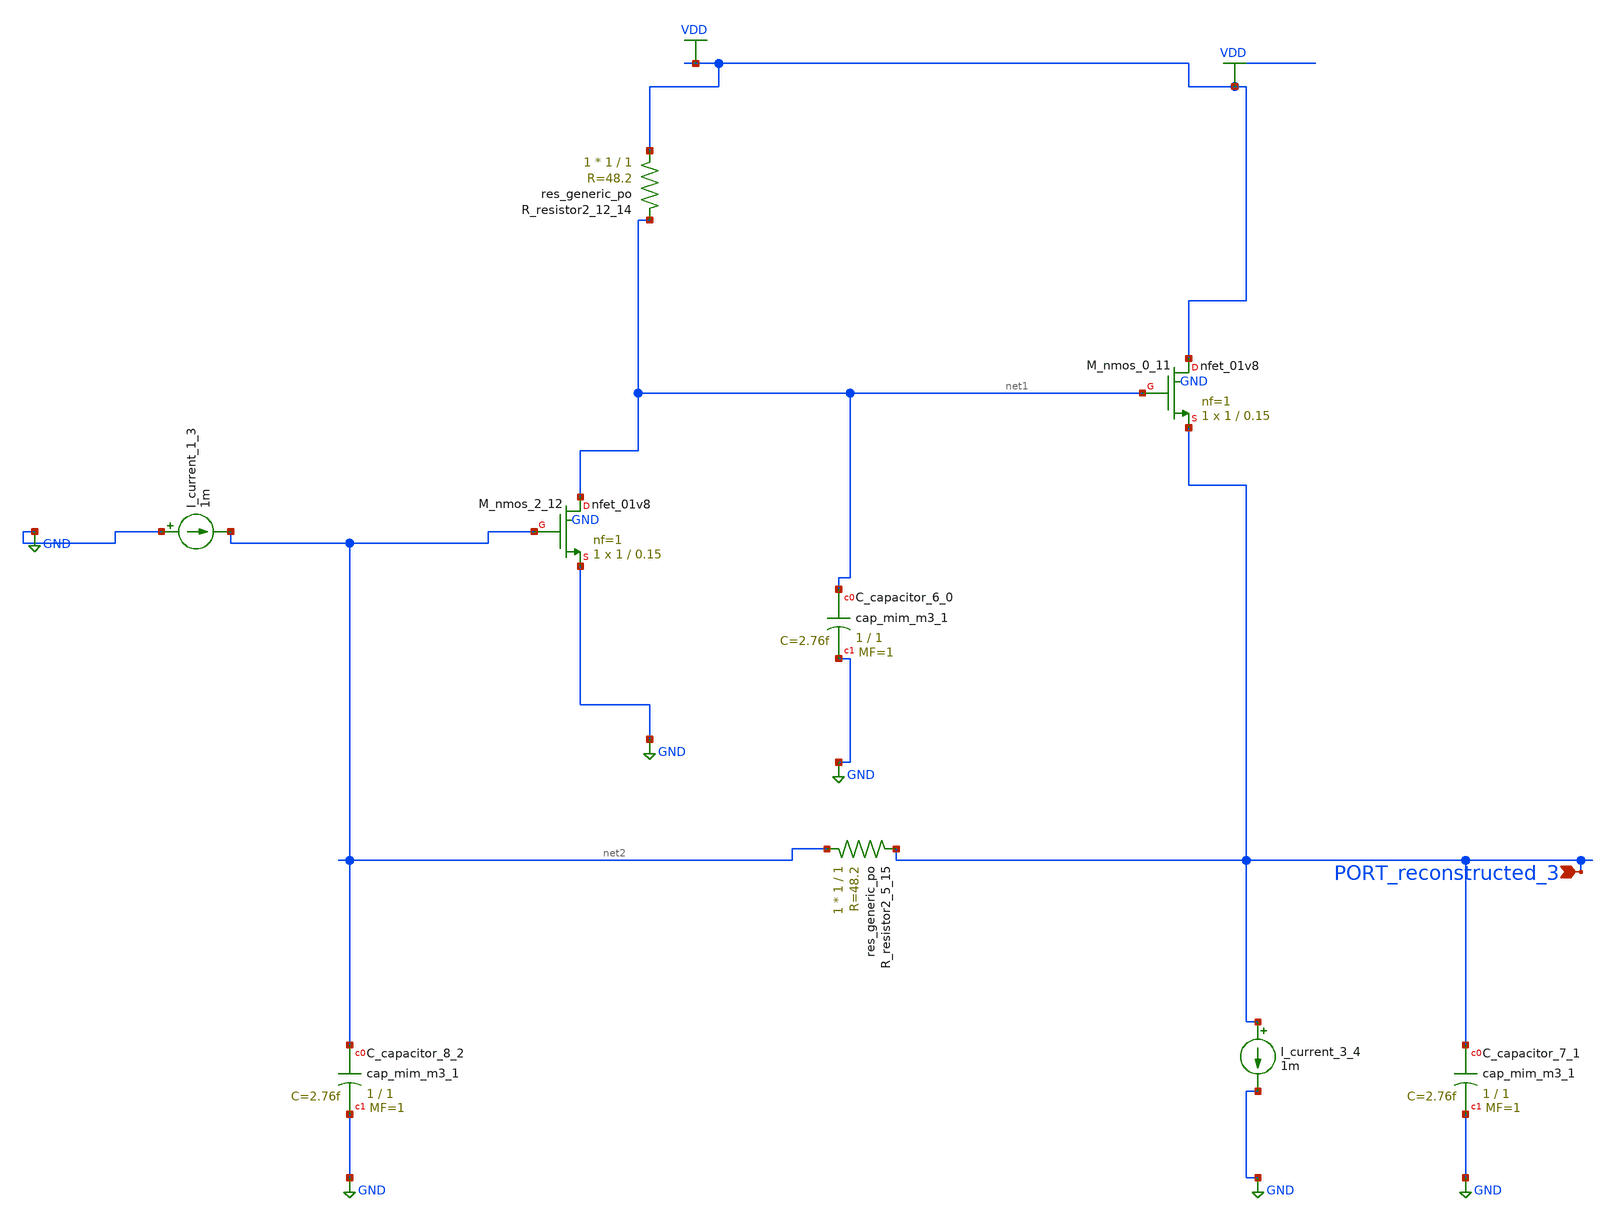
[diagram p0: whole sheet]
** sch_path: schematics/AMSNet/740.sch
**.subckt 740 PORT_reconstructed_3
*.ipin PORT_reconstructed_3
XC_capacitor_6_0 net1 GND sky130_fd_pr__cap_mim_m3_1 W=1 L=1 MF=1 m=1
XC_capacitor_7_1 PORT_reconstructed_3 GND sky130_fd_pr__cap_mim_m3_1 W=1 L=1 MF=1 m=1
XC_capacitor_8_2 net2 GND sky130_fd_pr__cap_mim_m3_1 W=1 L=1 MF=1 m=1
I_current_1_3 GND net2 1m
I_current_3_4 PORT_reconstructed_3 GND 1m
XM_nmos_0_11 VDD net1 PORT_reconstructed_3 GND sky130_fd_pr__nfet_01v8 L=0.15 W=1 nf=1 ad='int((1 + 1)/2) * 1 / 1 * 0.29'
+ as='int((1 + 2)/2) * 1 / 1 * 0.29' pd='2*int((1 + 1)/2) * (1 / 1 + 0.29)' ps='2*int((1 + 2)/2) * (1 / 1 + 0.29)'
+ nrd='0.29 / 1 ' nrs='0.29 / 1 ' sa=0 sb=0 sd=0 mult=1 m=1
XM_nmos_2_12 net1 net2 GND GND sky130_fd_pr__nfet_01v8 L=0.15 W=1 nf=1 ad='int((1 + 1)/2) * 1 / 1 * 0.29'
+ as='int((1 + 2)/2) * 1 / 1 * 0.29' pd='2*int((1 + 1)/2) * (1 / 1 + 0.29)' ps='2*int((1 + 2)/2) * (1 / 1 + 0.29)'
+ nrd='0.29 / 1 ' nrs='0.29 / 1 ' sa=0 sb=0 sd=0 mult=1 m=1
XR_resistor2_12_14 VDD net1 sky130_fd_pr__res_generic_po W=1 L=1 m=1
XR_resistor2_5_15 net2 PORT_reconstructed_3 sky130_fd_pr__res_generic_po W=1 L=1 m=1
**.ends
.GLOBAL GND
.GLOBAL VDD
.end
